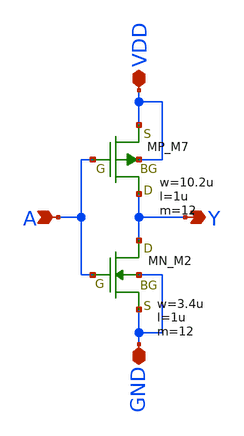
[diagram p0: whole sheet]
** sch_path: libs.tech/xschem/TR-1um_5_stdcell/INV_X12.sch
**.subckt INV_X12 A Y GND VDD
*.ipin A
*.opin Y
*.iopin GND
*.iopin VDD
XM7 Y A VDD VDD PMOS w=10.2u l=1u nrd=0 nrs=0 m=12
XM2 Y A GND GND NMOS w=3.4u l=1u nrd=0 nrs=0 m=12
**.ends
.end
